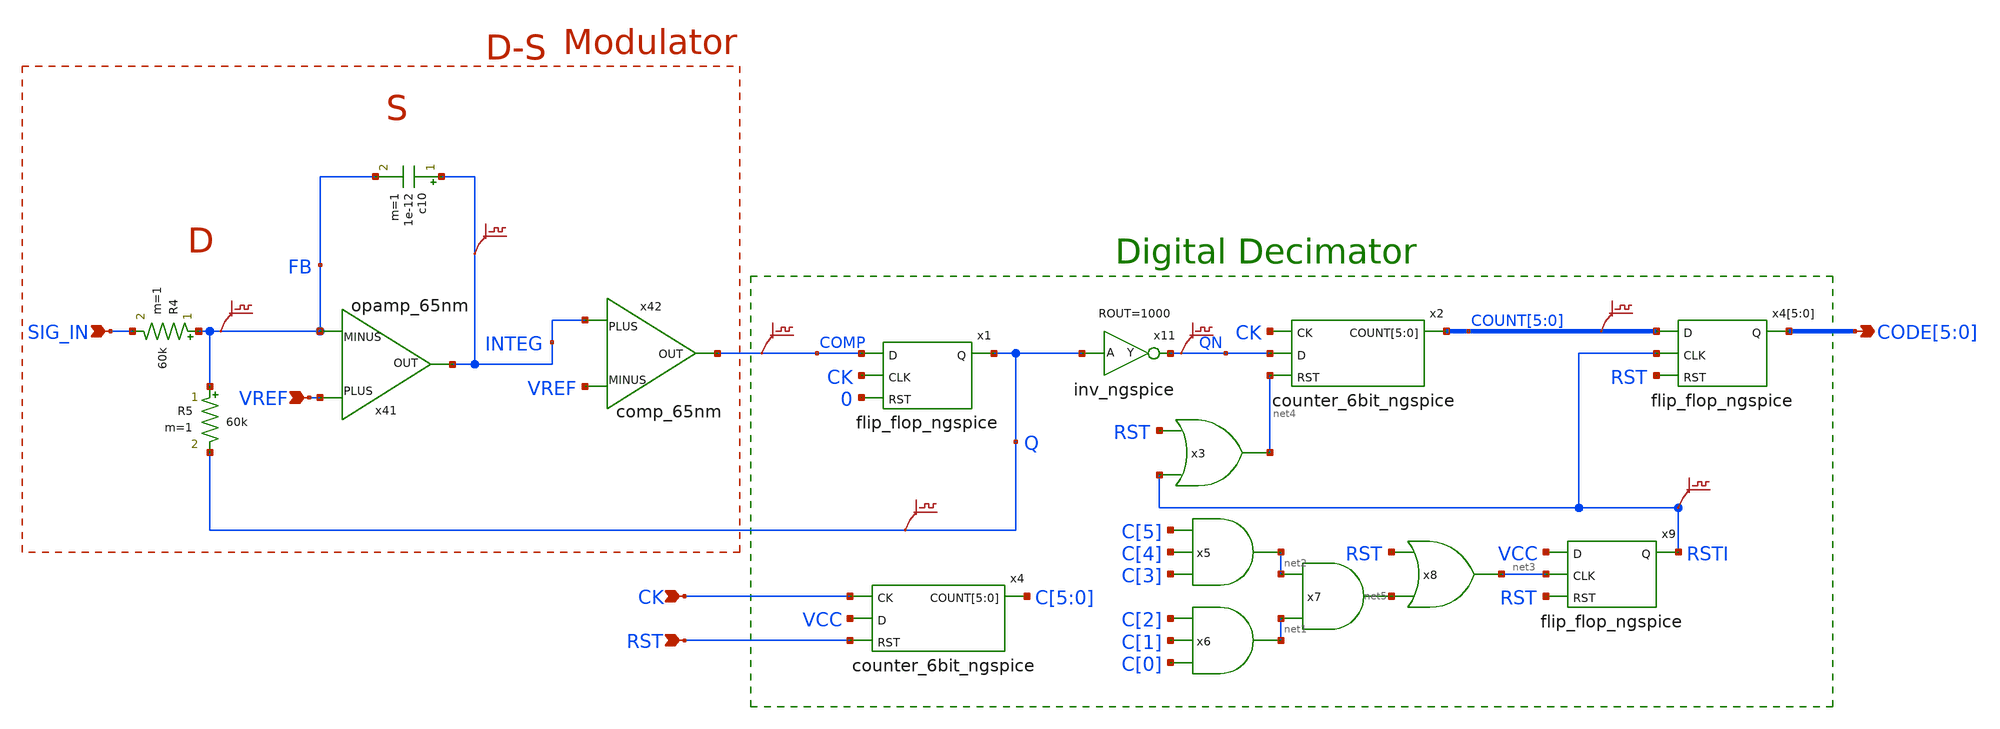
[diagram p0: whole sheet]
** sch_path: xschem_libraries_oa/ngspice/adc/schematic/adc.sch
* Copyright (C) 1998-2024 Stefan Frederik Schippers
* This program is free software; you can redistribute it and/or modify
* it under the terms of the GNU General Public License as published by
* the Free Software Foundation; either version 2 of the License, or
* (at your option) any later version.
* This program is distributed in the hope that it will be useful,
* but WITHOUT ANY WARRANTY; without even the implied warranty of
* MERCHANTABILITY or FITNESS FOR A PARTICULAR PURPOSE.  See the
* GNU General Public License for more details.
* You should have received a copy of the GNU General Public License
* along with this program; if not, write to the Free Software
**.subckt adc CODE[5],CODE[4],CODE[3],CODE[2],CODE[1],CODE[0] CK RST VREF SIG_IN
*.opin CODE[5],CODE[4],CODE[3],CODE[2],CODE[1],CODE[0]
*.ipin CK
*.ipin RST
*.ipin VREF
*.ipin SIG_IN
x1 COMP CK Q 0 flip_flop_ngspice
x2 CK COUNT[5] COUNT[4] COUNT[3] COUNT[2] COUNT[1] COUNT[0] QN net4 counter_6bit_ngspice
x4[5] COUNT[5] RSTI CODE[5] RST flip_flop_ngspice
x4[4] COUNT[4] RSTI CODE[4] RST flip_flop_ngspice
x4[3] COUNT[3] RSTI CODE[3] RST flip_flop_ngspice
x4[2] COUNT[2] RSTI CODE[2] RST flip_flop_ngspice
x4[1] COUNT[1] RSTI CODE[1] RST flip_flop_ngspice
x4[0] COUNT[0] RSTI CODE[0] RST flip_flop_ngspice
x4 CK C[5] C[4] C[3] C[2] C[1] C[0] VCC RST counter_6bit_ngspice
x5 net2 C[5] C[4] C[3] and3_ngspice ROUT=1000
x6 net1 C[2] C[1] C[0] and3_ngspice ROUT=1000
x7 net5 net2 net1 and_ngspice ROUT=1000
x8 net3 RST net5 or_ngspice ROUT=1000
x9 VCC net3 RSTI RST flip_flop_ngspice
.save v(q)
.save v(comp)
.save v(rsti)
x11 QN Q inv_ngspice ROUT=1000
.save v(qn)
c10 INTEG FB 1e-12 m=1
R4 FB SIG_IN 60k m=1
R5 FB Q 60k m=1
.save v(integ)
.save v(fb)
x41 VREF INTEG FB opamp_65nm
x42 INTEG COMP VREF comp_65nm
.save v(count[5])
.save v(count[4])
.save v(count[3])
.save v(count[2])
.save v(count[1])
.save v(count[0])
x3 net4 RST RSTI or_ngspice ROUT=1000
**.ends
.end
